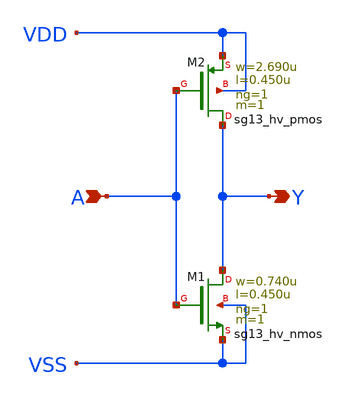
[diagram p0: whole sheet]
** sch_path: ihp-sg13g2/libs.ref/sg13g2_stdcell_hv/sch/xschem/sg13g2_hv_inv_1.sch
* Copyright 2023 IHP PDK Authors
* Licensed under the Apache License, Version 2.0 (the "License");
* you may not use this file except in compliance with the License.
* You may obtain a copy of the License at
* https://www.apache.org/licenses/LICENSE-2.0
* Unless required by applicable law or agreed to in writing, software
* distributed under the License is distributed on an "AS IS" BASIS,
* WITHOUT WARRANTIES OR CONDITIONS OF ANY KIND, either express or implied.
* See the License for the specific language governing permissions and
* limitations under the License.
**.subckt sg13g2_hv_inv_1 Y A
*.opin Y
*.ipin A
XM1 Y A VSS VSS sg13_hv_nmos w=0.740u l=0.450u ng=1 m=1 mm_ok=1
XM2 Y A VDD VDD sg13_hv_pmos w=2.690u l=0.450u ng=1 m=1 mm_ok=1
**.ends
.end
